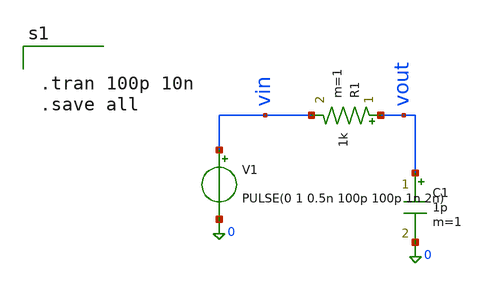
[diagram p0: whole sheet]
** sch_path: RC_Circuit.sch
**.subckt RC_Circuit
R1 vout vin 1k m=1
V1 vin 0 PULSE(0 1 0.5n 100p 100p 1n 2n)
C1 vout 0 1p m=1
**** begin user architecture code


.tran 100p 10n
.save all


**** end user architecture code
**.ends
.end
